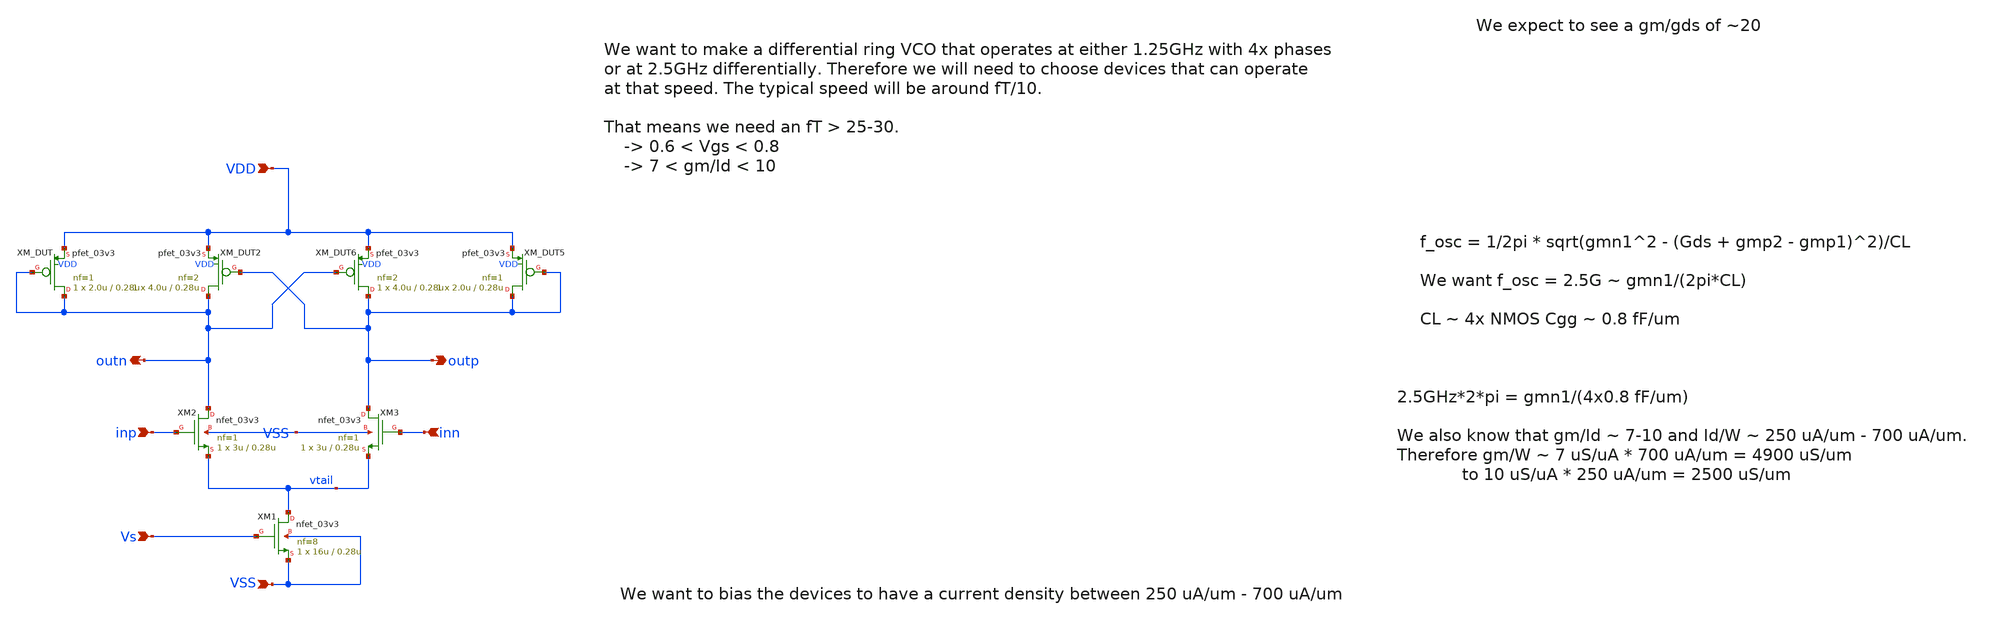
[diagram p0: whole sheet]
** sch_path: xschem/delay_cell_v1.sch
**.subckt delay_cell_v1 inp inn outp outn VDD VSS Vs
*.ipin inp
*.ipin inn
*.opin outp
*.opin outn
*.ipin VDD
*.ipin VSS
*.ipin Vs
XM_DUT outn outn VDD VDD pfet_03v3 L=0.28u W=2.0u nf=1 ad='int((nf+1)/2) * W/nf * 0.18u' as='int((nf+2)/2) * W/nf * 0.18u'
+ pd='2*int((nf+1)/2) * (W/nf + 0.18u)' ps='2*int((nf+2)/2) * (W/nf + 0.18u)' nrd='0.18u / W' nrs='0.18u / W'
+ sa=0 sb=0 sd=0 m=1 par=1
XM1 vtail Vs VSS VSS nfet_03v3 L=0.28u W=16u nf=8 ad='int((nf+1)/2) * W/nf * 0.18u' as='int((nf+2)/2) * W/nf * 0.18u'
+ pd='2*int((nf+1)/2) * (W/nf + 0.18u)' ps='2*int((nf+2)/2) * (W/nf + 0.18u)' nrd='0.18u / W' nrs='0.18u / W'
+ sa=0 sb=0 sd=0 m=1 par=1
XM_DUT2 outn outp VDD VDD pfet_03v3 L=0.28u W=4.0u nf=2 ad='int((nf+1)/2) * W/nf * 0.18u' as='int((nf+2)/2) * W/nf * 0.18u'
+ pd='2*int((nf+1)/2) * (W/nf + 0.18u)' ps='2*int((nf+2)/2) * (W/nf + 0.18u)' nrd='0.18u / W' nrs='0.18u / W'
+ sa=0 sb=0 sd=0 m=1 par=1
XM3 outp inn vtail VSS nfet_03v3 L=0.28u W=3u nf=1 ad='int((nf+1)/2) * W/nf * 0.18u' as='int((nf+2)/2) * W/nf * 0.18u'
+ pd='2*int((nf+1)/2) * (W/nf + 0.18u)' ps='2*int((nf+2)/2) * (W/nf + 0.18u)' nrd='0.18u / W' nrs='0.18u / W'
+ sa=0 sb=0 sd=0 m=1 par=1
XM2 outn inp vtail VSS nfet_03v3 L=0.28u W=3u nf=1 ad='int((nf+1)/2) * W/nf * 0.18u' as='int((nf+2)/2) * W/nf * 0.18u'
+ pd='2*int((nf+1)/2) * (W/nf + 0.18u)' ps='2*int((nf+2)/2) * (W/nf + 0.18u)' nrd='0.18u / W' nrs='0.18u / W'
+ sa=0 sb=0 sd=0 m=1 par=1
XM_DUT5 outp outp VDD VDD pfet_03v3 L=0.28u W=2.0u nf=1 ad='int((nf+1)/2) * W/nf * 0.18u' as='int((nf+2)/2) * W/nf * 0.18u'
+ pd='2*int((nf+1)/2) * (W/nf + 0.18u)' ps='2*int((nf+2)/2) * (W/nf + 0.18u)' nrd='0.18u / W' nrs='0.18u / W'
+ sa=0 sb=0 sd=0 m=1 par=1
XM_DUT6 outp outn VDD VDD pfet_03v3 L=0.28u W=4.0u nf=2 ad='int((nf+1)/2) * W/nf * 0.18u' as='int((nf+2)/2) * W/nf * 0.18u'
+ pd='2*int((nf+1)/2) * (W/nf + 0.18u)' ps='2*int((nf+2)/2) * (W/nf + 0.18u)' nrd='0.18u / W' nrs='0.18u / W'
+ sa=0 sb=0 sd=0 m=1 par=1
**.ends
.end
